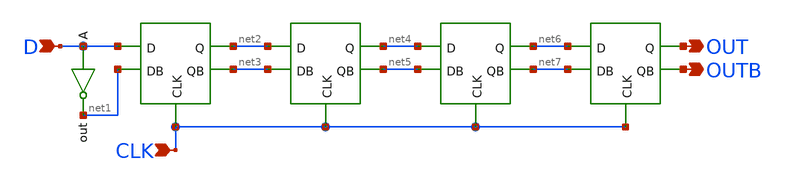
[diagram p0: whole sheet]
** sch_path: MP2/4bitShiftReg_tile.sch
**.subckt 4bitShiftReg_tile OUT OUTB D CLK
*.opin OUT
*.opin OUTB
*.ipin D
*.ipin CLK
x1 D net2 net1 net3 CLK DFF
x2 net2 net4 net3 net5 CLK DFF
x3 net4 net6 net5 net7 CLK DFF
x4 net6 OUT net7 OUTB CLK DFF
x5 net1 D INV_mp1
**.ends

* expanding   symbol:  /home/madvlsi/Documents/MP2/DFF.sym # of pins=5
** sym_path: MP2/DFF.sym
** sch_path: MP2/DFF.sch
.subckt DFF D Q DB QB CLK
*.ipin D
*.ipin DB
*.ipin CLK
*.opin Q
*.opin QB
XM1 net1 CLK D VDD sky130_fd_pr__pfet_01v8 L=0.15 W=1 nf=1 ad='int((nf+1)/2) * W/nf * 0.29' as='int((nf+2)/2) * W/nf * 0.29'
+ pd='2*int((nf+1)/2) * (W/nf + 0.29)' ps='2*int((nf+2)/2) * (W/nf + 0.29)' nrd='0.29 / W' nrs='0.29 / W'
+ sa=0 sb=0 sd=0 mult=1 m=1
XM2 net2 CLK DB VDD sky130_fd_pr__pfet_01v8 L=0.15 W=1 nf=1 ad='int((nf+1)/2) * W/nf * 0.29' as='int((nf+2)/2) * W/nf * 0.29'
+ pd='2*int((nf+1)/2) * (W/nf + 0.29)' ps='2*int((nf+2)/2) * (W/nf + 0.29)' nrd='0.29 / W' nrs='0.29 / W'
+ sa=0 sb=0 sd=0 mult=1 m=1
XM3 Q CLK net1 GND sky130_fd_pr__nfet_01v8 L=0.15 W=1 nf=1 ad='int((nf+1)/2) * W/nf * 0.29' as='int((nf+2)/2) * W/nf * 0.29'
+ pd='2*int((nf+1)/2) * (W/nf + 0.29)' ps='2*int((nf+2)/2) * (W/nf + 0.29)' nrd='0.29 / W' nrs='0.29 / W'
+ sa=0 sb=0 sd=0 mult=1 m=1
XM4 QB CLK net2 GND sky130_fd_pr__nfet_01v8 L=0.15 W=1 nf=1 ad='int((nf+1)/2) * W/nf * 0.29' as='int((nf+2)/2) * W/nf * 0.29'
+ pd='2*int((nf+1)/2) * (W/nf + 0.29)' ps='2*int((nf+2)/2) * (W/nf + 0.29)' nrd='0.29 / W' nrs='0.29 / W'
+ sa=0 sb=0 sd=0 mult=1 m=1
XM5 net3 CLK GND GND sky130_fd_pr__nfet_01v8 L=0.15 W=4 nf=1 ad='int((nf+1)/2) * W/nf * 0.29' as='int((nf+2)/2) * W/nf * 0.29'
+ pd='2*int((nf+1)/2) * (W/nf + 0.29)' ps='2*int((nf+2)/2) * (W/nf + 0.29)' nrd='0.29 / W' nrs='0.29 / W'
+ sa=0 sb=0 sd=0 mult=1 m=1
XM6 net2 net1 net3 GND sky130_fd_pr__nfet_01v8 L=0.15 W=1 nf=1 ad='int((nf+1)/2) * W/nf * 0.29' as='int((nf+2)/2) * W/nf * 0.29'
+ pd='2*int((nf+1)/2) * (W/nf + 0.29)' ps='2*int((nf+2)/2) * (W/nf + 0.29)' nrd='0.29 / W' nrs='0.29 / W'
+ sa=0 sb=0 sd=0 mult=1 m=1
XM7 net1 net2 net3 GND sky130_fd_pr__nfet_01v8 L=0.15 W=1 nf=1 ad='int((nf+1)/2) * W/nf * 0.29' as='int((nf+2)/2) * W/nf * 0.29'
+ pd='2*int((nf+1)/2) * (W/nf + 0.29)' ps='2*int((nf+2)/2) * (W/nf + 0.29)' nrd='0.29 / W' nrs='0.29 / W'
+ sa=0 sb=0 sd=0 mult=1 m=1
XM8 VDD net1 net2 VDD sky130_fd_pr__pfet_01v8 L=0.15 W=1 nf=1 ad='int((nf+1)/2) * W/nf * 0.29' as='int((nf+2)/2) * W/nf * 0.29'
+ pd='2*int((nf+1)/2) * (W/nf + 0.29)' ps='2*int((nf+2)/2) * (W/nf + 0.29)' nrd='0.29 / W' nrs='0.29 / W'
+ sa=0 sb=0 sd=0 mult=1 m=1
XM9 VDD net2 net1 VDD sky130_fd_pr__pfet_01v8 L=0.15 W=1 nf=1 ad='int((nf+1)/2) * W/nf * 0.29' as='int((nf+2)/2) * W/nf * 0.29'
+ pd='2*int((nf+1)/2) * (W/nf + 0.29)' ps='2*int((nf+2)/2) * (W/nf + 0.29)' nrd='0.29 / W' nrs='0.29 / W'
+ sa=0 sb=0 sd=0 mult=1 m=1
XM10 net4 CLK VDD VDD sky130_fd_pr__pfet_01v8 L=0.15 W=4 nf=1 ad='int((nf+1)/2) * W/nf * 0.29' as='int((nf+2)/2) * W/nf * 0.29'
+ pd='2*int((nf+1)/2) * (W/nf + 0.29)' ps='2*int((nf+2)/2) * (W/nf + 0.29)' nrd='0.29 / W' nrs='0.29 / W'
+ sa=0 sb=0 sd=0 mult=1 m=1
XM11 net4 Q QB VDD sky130_fd_pr__pfet_01v8 L=0.15 W=1 nf=1 ad='int((nf+1)/2) * W/nf * 0.29' as='int((nf+2)/2) * W/nf * 0.29'
+ pd='2*int((nf+1)/2) * (W/nf + 0.29)' ps='2*int((nf+2)/2) * (W/nf + 0.29)' nrd='0.29 / W' nrs='0.29 / W'
+ sa=0 sb=0 sd=0 mult=1 m=1
XM12 net4 QB Q VDD sky130_fd_pr__pfet_01v8 L=0.15 W=1 nf=1 ad='int((nf+1)/2) * W/nf * 0.29' as='int((nf+2)/2) * W/nf * 0.29'
+ pd='2*int((nf+1)/2) * (W/nf + 0.29)' ps='2*int((nf+2)/2) * (W/nf + 0.29)' nrd='0.29 / W' nrs='0.29 / W'
+ sa=0 sb=0 sd=0 mult=1 m=1
XM13 QB Q GND GND sky130_fd_pr__nfet_01v8 L=0.15 W=1 nf=1 ad='int((nf+1)/2) * W/nf * 0.29' as='int((nf+2)/2) * W/nf * 0.29'
+ pd='2*int((nf+1)/2) * (W/nf + 0.29)' ps='2*int((nf+2)/2) * (W/nf + 0.29)' nrd='0.29 / W' nrs='0.29 / W'
+ sa=0 sb=0 sd=0 mult=1 m=1
XM14 Q QB GND GND sky130_fd_pr__nfet_01v8 L=0.15 W=1 nf=1 ad='int((nf+1)/2) * W/nf * 0.29' as='int((nf+2)/2) * W/nf * 0.29'
+ pd='2*int((nf+1)/2) * (W/nf + 0.29)' ps='2*int((nf+2)/2) * (W/nf + 0.29)' nrd='0.29 / W' nrs='0.29 / W'
+ sa=0 sb=0 sd=0 mult=1 m=1
.ends


* expanding   symbol:  /home/madvlsi/Documents/MP1/INV_mp1.sym # of pins=2
** sym_path: MP1/INV_mp1.sym
** sch_path: MP1/INV_mp1.sch
.subckt INV_mp1 out A
*.ipin A
*.opin out
XM1 out A VDD VDD sky130_fd_pr__pfet_01v8 L=0.15 W=1 nf=1 ad='int((nf+1)/2) * W/nf * 0.29' as='int((nf+2)/2) * W/nf * 0.29'
+ pd='2*int((nf+1)/2) * (W/nf + 0.29)' ps='2*int((nf+2)/2) * (W/nf + 0.29)' nrd='0.29 / W' nrs='0.29 / W'
+ sa=0 sb=0 sd=0 mult=1 m=1
XM2 out A GND GND sky130_fd_pr__nfet_01v8 L=0.15 W=1 nf=1 ad='int((nf+1)/2) * W/nf * 0.29' as='int((nf+2)/2) * W/nf * 0.29'
+ pd='2*int((nf+1)/2) * (W/nf + 0.29)' ps='2*int((nf+2)/2) * (W/nf + 0.29)' nrd='0.29 / W' nrs='0.29 / W'
+ sa=0 sb=0 sd=0 mult=1 m=1
.ends

.GLOBAL VDD
.GLOBAL GND
.end
